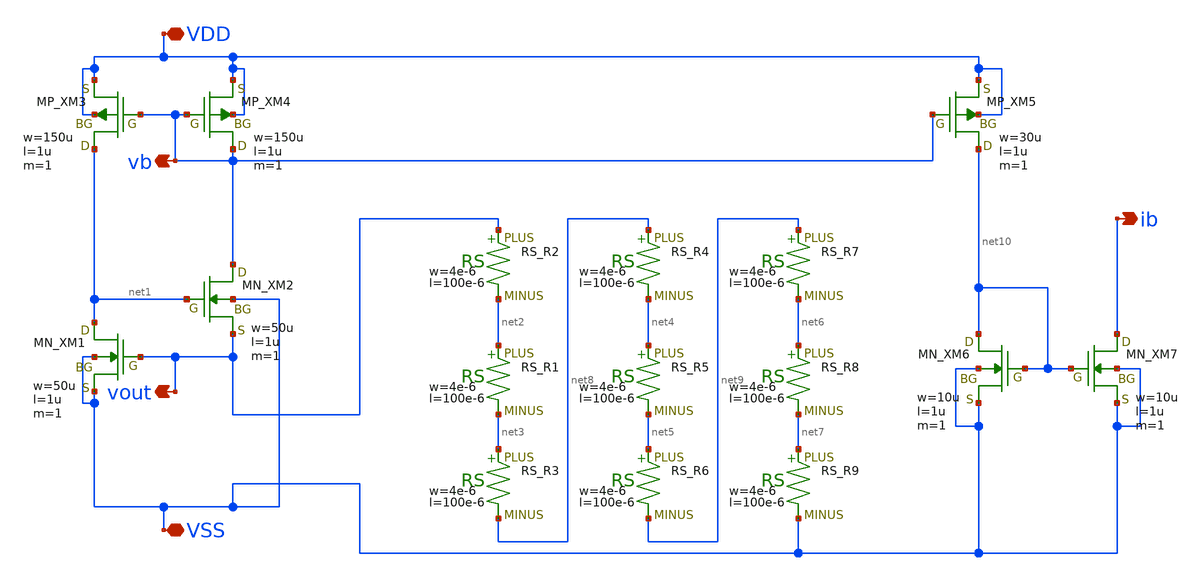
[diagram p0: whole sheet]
** sch_path: schematic/20250924_OSS_Workshop/ishikai/CS/cs-vth-ref.sch
**.subckt cs-vth-ref VSS VDD ib vb vout
*.iopin VSS
*.iopin VDD
*.opin ib
*.opin vb
*.opin vout
XM1 net1 vout VSS VSS NMOS w=50u l=1u as=0 ad=0 ps=0 pd=0 nrd=0 nrs=0 m=1
XM2 vb net1 vout VSS NMOS w=50u l=1u as=0 ad=0 ps=0 pd=0 nrd=0 nrs=0 m=1
XM3 net1 vb VDD VDD PMOS w=150u l=1u as=0 ad=0 ps=0 pd=0 nrd=0 nrs=0 m=1
XM4 vb vb VDD VDD PMOS w=150u l=1u as=0 ad=0 ps=0 pd=0 nrd=0 nrs=0 m=1
XR2 vout net2 F_RS w=4e-6 R=3000 l=100e-6 tc1=0 tc2=0
XR1 net2 net3 F_RS w=4e-6 R=3000 l=100e-6 tc1=0 tc2=0
XR3 net3 net8 F_RS w=4e-6 R=3000 l=100e-6 tc1=0 tc2=0
XR4 net8 net4 F_RS w=4e-6 R=3000 l=100e-6 tc1=0 tc2=0
XR5 net4 net5 F_RS w=4e-6 R=3000 l=100e-6 tc1=0 tc2=0
XR6 net5 net9 F_RS w=4e-6 R=3000 l=100e-6 tc1=0 tc2=0
XR7 net9 net6 F_RS w=4e-6 R=3000 l=100e-6 tc1=0 tc2=0
XR8 net6 net7 F_RS w=4e-6 R=3000 l=100e-6 tc1=0 tc2=0
XR9 net7 VSS F_RS w=4e-6 R=3000 l=100e-6 tc1=0 tc2=0
XM5 net10 vb VDD VDD PMOS w=30u l=1u as=0 ad=0 ps=0 pd=0 nrd=0 nrs=0 m=1
XM6 net10 net10 VSS VSS NMOS w=10u l=1u as=0 ad=0 ps=0 pd=0 nrd=0 nrs=0 m=1
XM7 ib net10 VSS VSS NMOS w=10u l=1u as=0 ad=0 ps=0 pd=0 nrd=0 nrs=0 m=1
**.ends
.end
